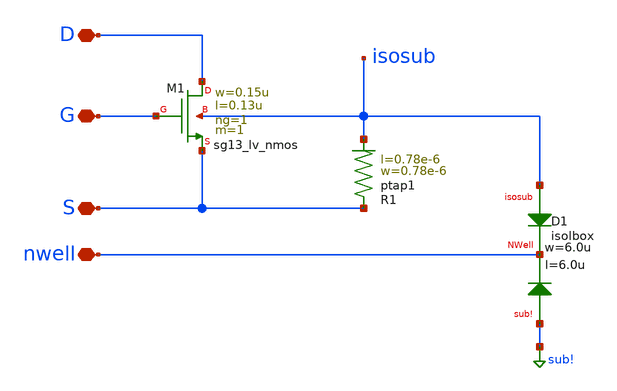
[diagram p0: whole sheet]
** sch_path: deepNWell/schematic/inmos.sch
**.subckt inmos D G S nwell
*.iopin D
*.iopin G
*.iopin S
*.iopin nwell
XM1 D G S isosub sg13_lv_nmos w=0.15u l=0.13u ng=1 m=1 mm_ok=1
XR1 S isosub ptap1 R=262.8 w=0.78e-6 l=0.78e-6
XD1 isosub nwell sub! isolbox l=6.0u w=6.0u
**.ends
.GLOBAL sub!
.end
